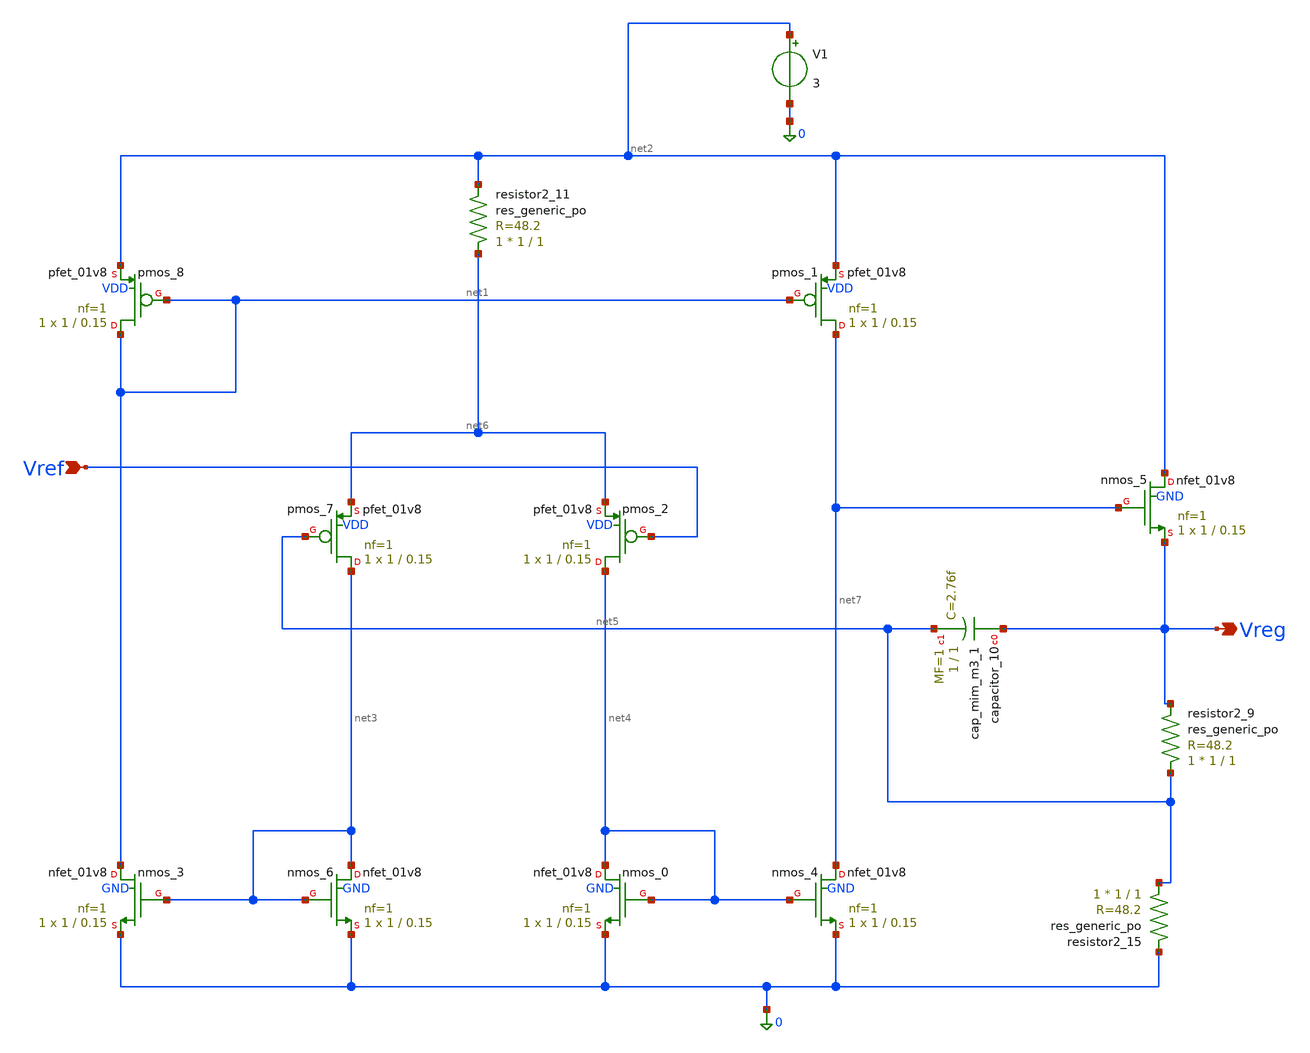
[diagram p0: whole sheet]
** sch_path: golden_netlists/10_1007_s00502-020-00859-w_04_001_crop1.sch
**.subckt 10_1007_s00502-020-00859-w_04_001_crop1 Vref Vreg
*.ipin Vref
*.opin Vreg
Xcapacitor_10 Vreg net5 sky130_fd_pr__cap_mim_m3_1 W=1 L=1 MF=1 m=1
Xnmos_0 net4 net4 0 GND sky130_fd_pr__nfet_01v8 L=0.15 W=1 nf=1 ad='int((nf+1)/2) * W/nf * 0.29' as='int((nf+2)/2) * W/nf * 0.29'
+ pd='2*int((nf+1)/2) * (W/nf + 0.29)' ps='2*int((nf+2)/2) * (W/nf + 0.29)' nrd='0.29 / W' nrs='0.29 / W'
+ sa=0 sb=0 sd=0 mult=1 m=1
Xnmos_3 net1 net3 0 GND sky130_fd_pr__nfet_01v8 L=0.15 W=1 nf=1 ad='int((nf+1)/2) * W/nf * 0.29' as='int((nf+2)/2) * W/nf * 0.29'
+ pd='2*int((nf+1)/2) * (W/nf + 0.29)' ps='2*int((nf+2)/2) * (W/nf + 0.29)' nrd='0.29 / W' nrs='0.29 / W'
+ sa=0 sb=0 sd=0 mult=1 m=1
Xnmos_4 net7 net4 0 GND sky130_fd_pr__nfet_01v8 L=0.15 W=1 nf=1 ad='int((nf+1)/2) * W/nf * 0.29' as='int((nf+2)/2) * W/nf * 0.29'
+ pd='2*int((nf+1)/2) * (W/nf + 0.29)' ps='2*int((nf+2)/2) * (W/nf + 0.29)' nrd='0.29 / W' nrs='0.29 / W'
+ sa=0 sb=0 sd=0 mult=1 m=1
Xnmos_5 net2 net7 Vreg GND sky130_fd_pr__nfet_01v8 L=0.15 W=1 nf=1 ad='int((nf+1)/2) * W/nf * 0.29' as='int((nf+2)/2) * W/nf * 0.29'
+ pd='2*int((nf+1)/2) * (W/nf + 0.29)' ps='2*int((nf+2)/2) * (W/nf + 0.29)' nrd='0.29 / W' nrs='0.29 / W'
+ sa=0 sb=0 sd=0 mult=1 m=1
Xnmos_6 net3 net3 0 GND sky130_fd_pr__nfet_01v8 L=0.15 W=1 nf=1 ad='int((nf+1)/2) * W/nf * 0.29' as='int((nf+2)/2) * W/nf * 0.29'
+ pd='2*int((nf+1)/2) * (W/nf + 0.29)' ps='2*int((nf+2)/2) * (W/nf + 0.29)' nrd='0.29 / W' nrs='0.29 / W'
+ sa=0 sb=0 sd=0 mult=1 m=1
Xpmos_1 net7 net1 net2 VDD sky130_fd_pr__pfet_01v8 L=0.15 W=1 nf=1 ad='int((1 + 1)/2) * 1 / 1 * 0.29'
+ as='int((1 + 2)/2) * 1 / 1 * 0.29' pd='2*int((1 + 1)/2) * (1 / 1 + 0.29)' ps='2*int((1 + 2)/2) * (1 / 1 + 0.29)'
+ nrd='0.29 / 1 ' nrs='0.29 / 1 ' sa=0 sb=0 sd=0 mult=1 m=1
Xpmos_2 net4 Vref net6 VDD sky130_fd_pr__pfet_01v8 L=0.15 W=1 nf=1 ad='int((1 + 1)/2) * 1 / 1 * 0.29'
+ as='int((1 + 2)/2) * 1 / 1 * 0.29' pd='2*int((1 + 1)/2) * (1 / 1 + 0.29)' ps='2*int((1 + 2)/2) * (1 / 1 + 0.29)'
+ nrd='0.29 / 1 ' nrs='0.29 / 1 ' sa=0 sb=0 sd=0 mult=1 m=1
Xpmos_7 net3 net5 net6 VDD sky130_fd_pr__pfet_01v8 L=0.15 W=1 nf=1 ad='int((1 + 1)/2) * 1 / 1 * 0.29'
+ as='int((1 + 2)/2) * 1 / 1 * 0.29' pd='2*int((1 + 1)/2) * (1 / 1 + 0.29)' ps='2*int((1 + 2)/2) * (1 / 1 + 0.29)'
+ nrd='0.29 / 1 ' nrs='0.29 / 1 ' sa=0 sb=0 sd=0 mult=1 m=1
Xpmos_8 net1 net1 net2 VDD sky130_fd_pr__pfet_01v8 L=0.15 W=1 nf=1 ad='int((1 + 1)/2) * 1 / 1 * 0.29'
+ as='int((1 + 2)/2) * 1 / 1 * 0.29' pd='2*int((1 + 1)/2) * (1 / 1 + 0.29)' ps='2*int((1 + 2)/2) * (1 / 1 + 0.29)'
+ nrd='0.29 / 1 ' nrs='0.29 / 1 ' sa=0 sb=0 sd=0 mult=1 m=1
Xresistor2_11 net6 net2 sky130_fd_pr__res_generic_po W=1 L=1 m=1
Xresistor2_15 net5 0 sky130_fd_pr__res_generic_po W=1 L=1 m=1
Xresistor2_9 net5 Vreg sky130_fd_pr__res_generic_po W=1 L=1 m=1
V1 net2 0 3
**.ends
.end
